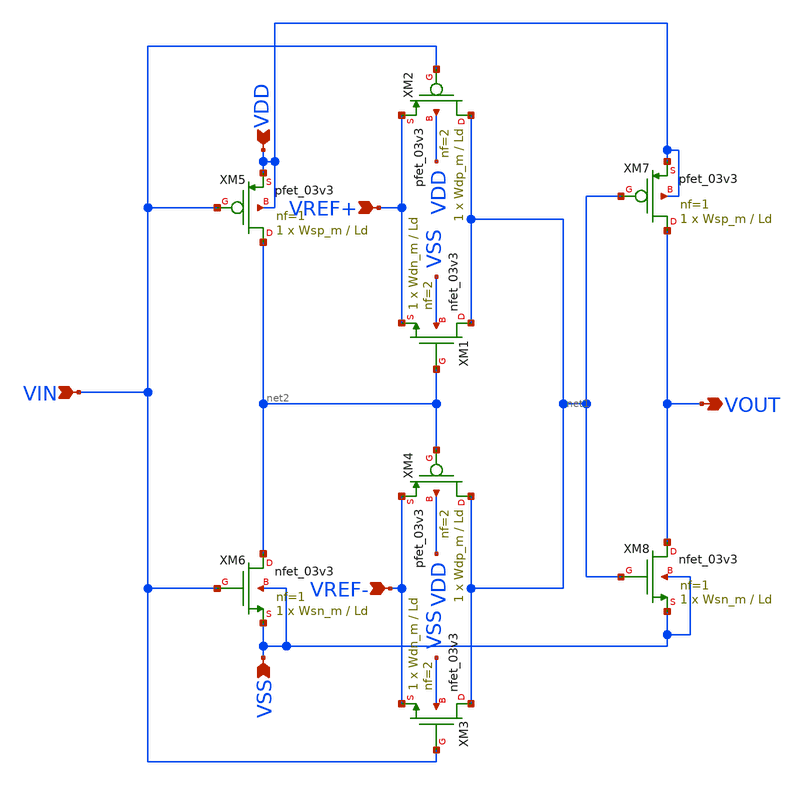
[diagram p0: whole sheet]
** sch_path: src/schematics/dac_1bit/DAC_1_BIT_MIN.sch
**.subckt DAC_1_BIT_MIN VIN VREF+ VREF- VOUT VDD VSS
*.ipin VIN
*.ipin VREF+
*.ipin VREF-
*.opin VOUT
*.ipin VDD
*.ipin VSS
XM1 net1 net2 VREF+ VSS nfet_03v3 L=Ld W=Wdn_m nf=2 ad='int((nf+1)/2) * W/nf * 0.18u' as='int((nf+2)/2) * W/nf * 0.18u'
+ pd='2*int((nf+1)/2) * (W/nf + 0.18u)' ps='2*int((nf+2)/2) * (W/nf + 0.18u)' nrd='0.18u / W' nrs='0.18u / W'
+ sa=0 sb=0 sd=0 m=1
XM2 net1 VIN VREF+ VDD pfet_03v3 L=Ld W=Wdp_m nf=2 ad='int((nf+1)/2) * W/nf * 0.18u' as='int((nf+2)/2) * W/nf * 0.18u'
+ pd='2*int((nf+1)/2) * (W/nf + 0.18u)' ps='2*int((nf+2)/2) * (W/nf + 0.18u)' nrd='0.18u / W' nrs='0.18u / W'
+ sa=0 sb=0 sd=0 m=1
XM3 net1 VIN VREF- VSS nfet_03v3 L=Ld W=Wdn_m nf=2 ad='int((nf+1)/2) * W/nf * 0.18u' as='int((nf+2)/2) * W/nf * 0.18u'
+ pd='2*int((nf+1)/2) * (W/nf + 0.18u)' ps='2*int((nf+2)/2) * (W/nf + 0.18u)' nrd='0.18u / W' nrs='0.18u / W'
+ sa=0 sb=0 sd=0 m=1
XM4 net1 net2 VREF- VDD pfet_03v3 L=Ld W=Wdp_m nf=2 ad='int((nf+1)/2) * W/nf * 0.18u' as='int((nf+2)/2) * W/nf * 0.18u'
+ pd='2*int((nf+1)/2) * (W/nf + 0.18u)' ps='2*int((nf+2)/2) * (W/nf + 0.18u)' nrd='0.18u / W' nrs='0.18u / W'
+ sa=0 sb=0 sd=0 m=1
XM5 net2 VIN VDD VDD pfet_03v3 L=Ld W=Wsp_m nf=1 ad='int((nf+1)/2) * W/nf * 0.18u' as='int((nf+2)/2) * W/nf * 0.18u'
+ pd='2*int((nf+1)/2) * (W/nf + 0.18u)' ps='2*int((nf+2)/2) * (W/nf + 0.18u)' nrd='0.18u / W' nrs='0.18u / W'
+ sa=0 sb=0 sd=0 m=1
XM6 net2 VIN VSS VSS nfet_03v3 L=Ld W=Wsn_m nf=1 ad='int((nf+1)/2) * W/nf * 0.18u' as='int((nf+2)/2) * W/nf * 0.18u'
+ pd='2*int((nf+1)/2) * (W/nf + 0.18u)' ps='2*int((nf+2)/2) * (W/nf + 0.18u)' nrd='0.18u / W' nrs='0.18u / W'
+ sa=0 sb=0 sd=0 m=1
XM7 VOUT net1 VDD VDD pfet_03v3 L=Ld W=Wsp_m nf=1 ad='int((nf+1)/2) * W/nf * 0.18u' as='int((nf+2)/2) * W/nf * 0.18u'
+ pd='2*int((nf+1)/2) * (W/nf + 0.18u)' ps='2*int((nf+2)/2) * (W/nf + 0.18u)' nrd='0.18u / W' nrs='0.18u / W'
+ sa=0 sb=0 sd=0 m=1
XM8 VOUT net1 VSS VSS nfet_03v3 L=Ld W=Wsn_m nf=1 ad='int((nf+1)/2) * W/nf * 0.18u' as='int((nf+2)/2) * W/nf * 0.18u'
+ pd='2*int((nf+1)/2) * (W/nf + 0.18u)' ps='2*int((nf+2)/2) * (W/nf + 0.18u)' nrd='0.18u / W' nrs='0.18u / W'
+ sa=0 sb=0 sd=0 m=1
**.ends
.end
